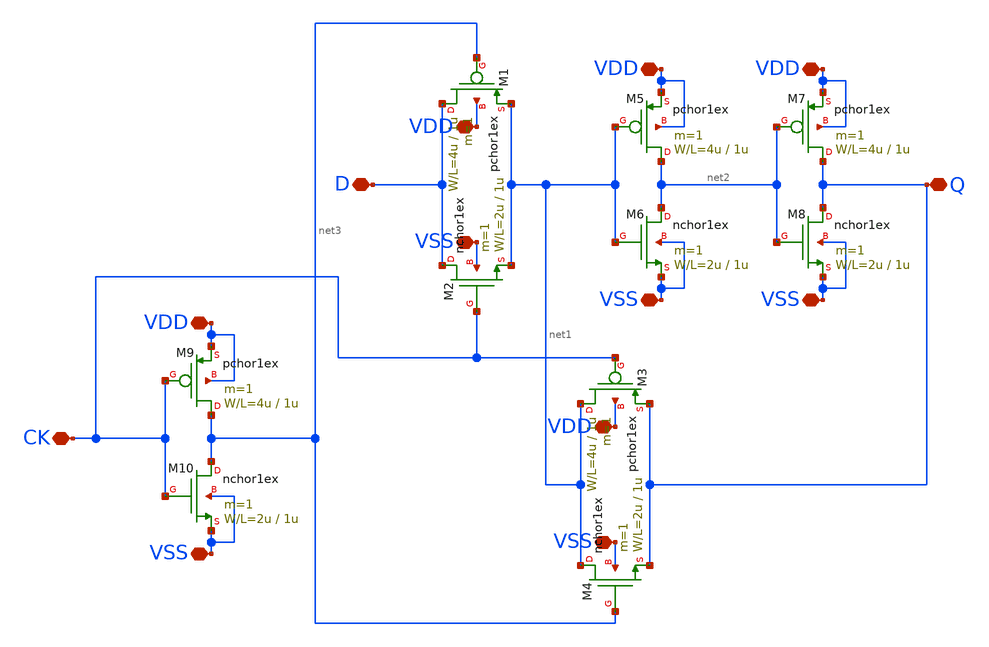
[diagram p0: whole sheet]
** sch_path: member_project/dokunira/Dlatch_layout/Dlatch.sch
**.subckt Dlatch CK D VDD VSS VDD VSS VDD VSS Q VDD VSS VDD VSS
*.iopin CK
*.iopin D
*.iopin VDD
*.iopin VSS
*.iopin VDD
*.iopin VSS
*.iopin VDD
*.iopin VSS
*.iopin Q
*.iopin VDD
*.iopin VSS
*.iopin VDD
*.iopin VSS
M1 D net3 net1 VDD pchor1ex L=1u W=4u m=1
M2 D CK net1 VSS nchor1ex L=1u W=2u m=1
M3 net1 CK Q VDD pchor1ex L=1u W=4u m=1
M4 net1 net3 Q VSS nchor1ex L=1u W=2u m=1
M5 net2 net1 VDD VDD pchor1ex L=1u W=4u m=1
M6 net2 net1 VSS VSS nchor1ex L=1u W=2u m=1
M7 Q net2 VDD VDD pchor1ex L=1u W=4u m=1
M8 Q net2 VSS VSS nchor1ex L=1u W=2u m=1
M9 net3 CK VDD VDD pchor1ex L=1u W=4u m=1
M10 net3 CK VSS VSS nchor1ex L=1u W=2u m=1
**.ends
.end
